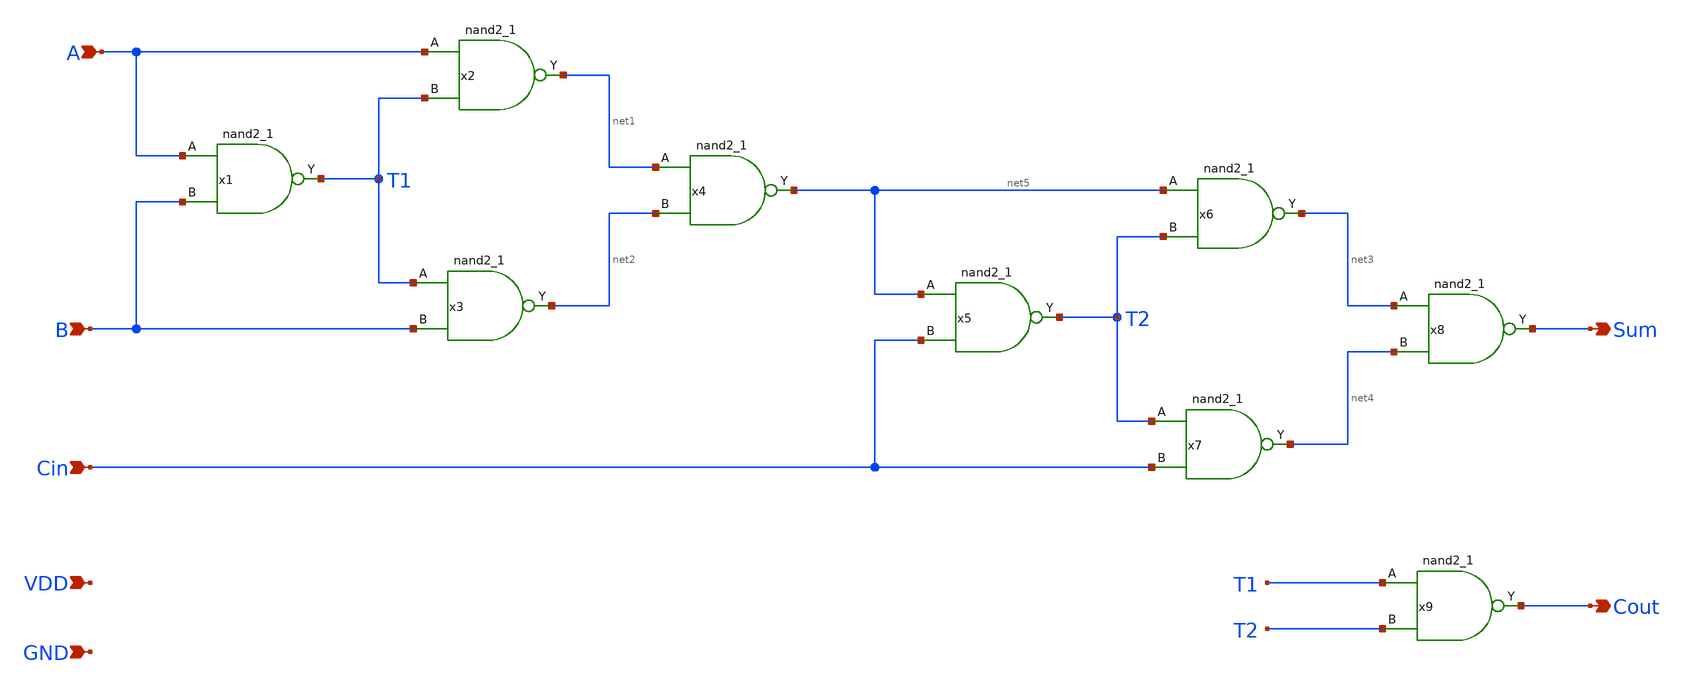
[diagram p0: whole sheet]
** sch_path: xschem/adder_1bit.sch
**.subckt adder_1bit A B Cin Sum Cout VDD GND
*.ipin A
*.ipin B
*.ipin Cin
*.opin Sum
*.opin Cout
*.ipin VDD
*.ipin GND
x1 A B GND GND VDD VDD T1 sky130_fd_sc_hd__nand2_1
x2 A T1 GND GND VDD VDD net1 sky130_fd_sc_hd__nand2_1
x3 T1 B GND GND VDD VDD net2 sky130_fd_sc_hd__nand2_1
x4 net1 net2 GND GND VDD VDD net5 sky130_fd_sc_hd__nand2_1
x5 net5 Cin GND GND VDD VDD T2 sky130_fd_sc_hd__nand2_1
x6 net5 T2 GND GND VDD VDD net3 sky130_fd_sc_hd__nand2_1
x7 T2 Cin GND GND VDD VDD net4 sky130_fd_sc_hd__nand2_1
x8 net3 net4 GND GND VDD VDD Sum sky130_fd_sc_hd__nand2_1
x9 T1 T2 GND GND VDD VDD Cout sky130_fd_sc_hd__nand2_1
**.ends
.end
